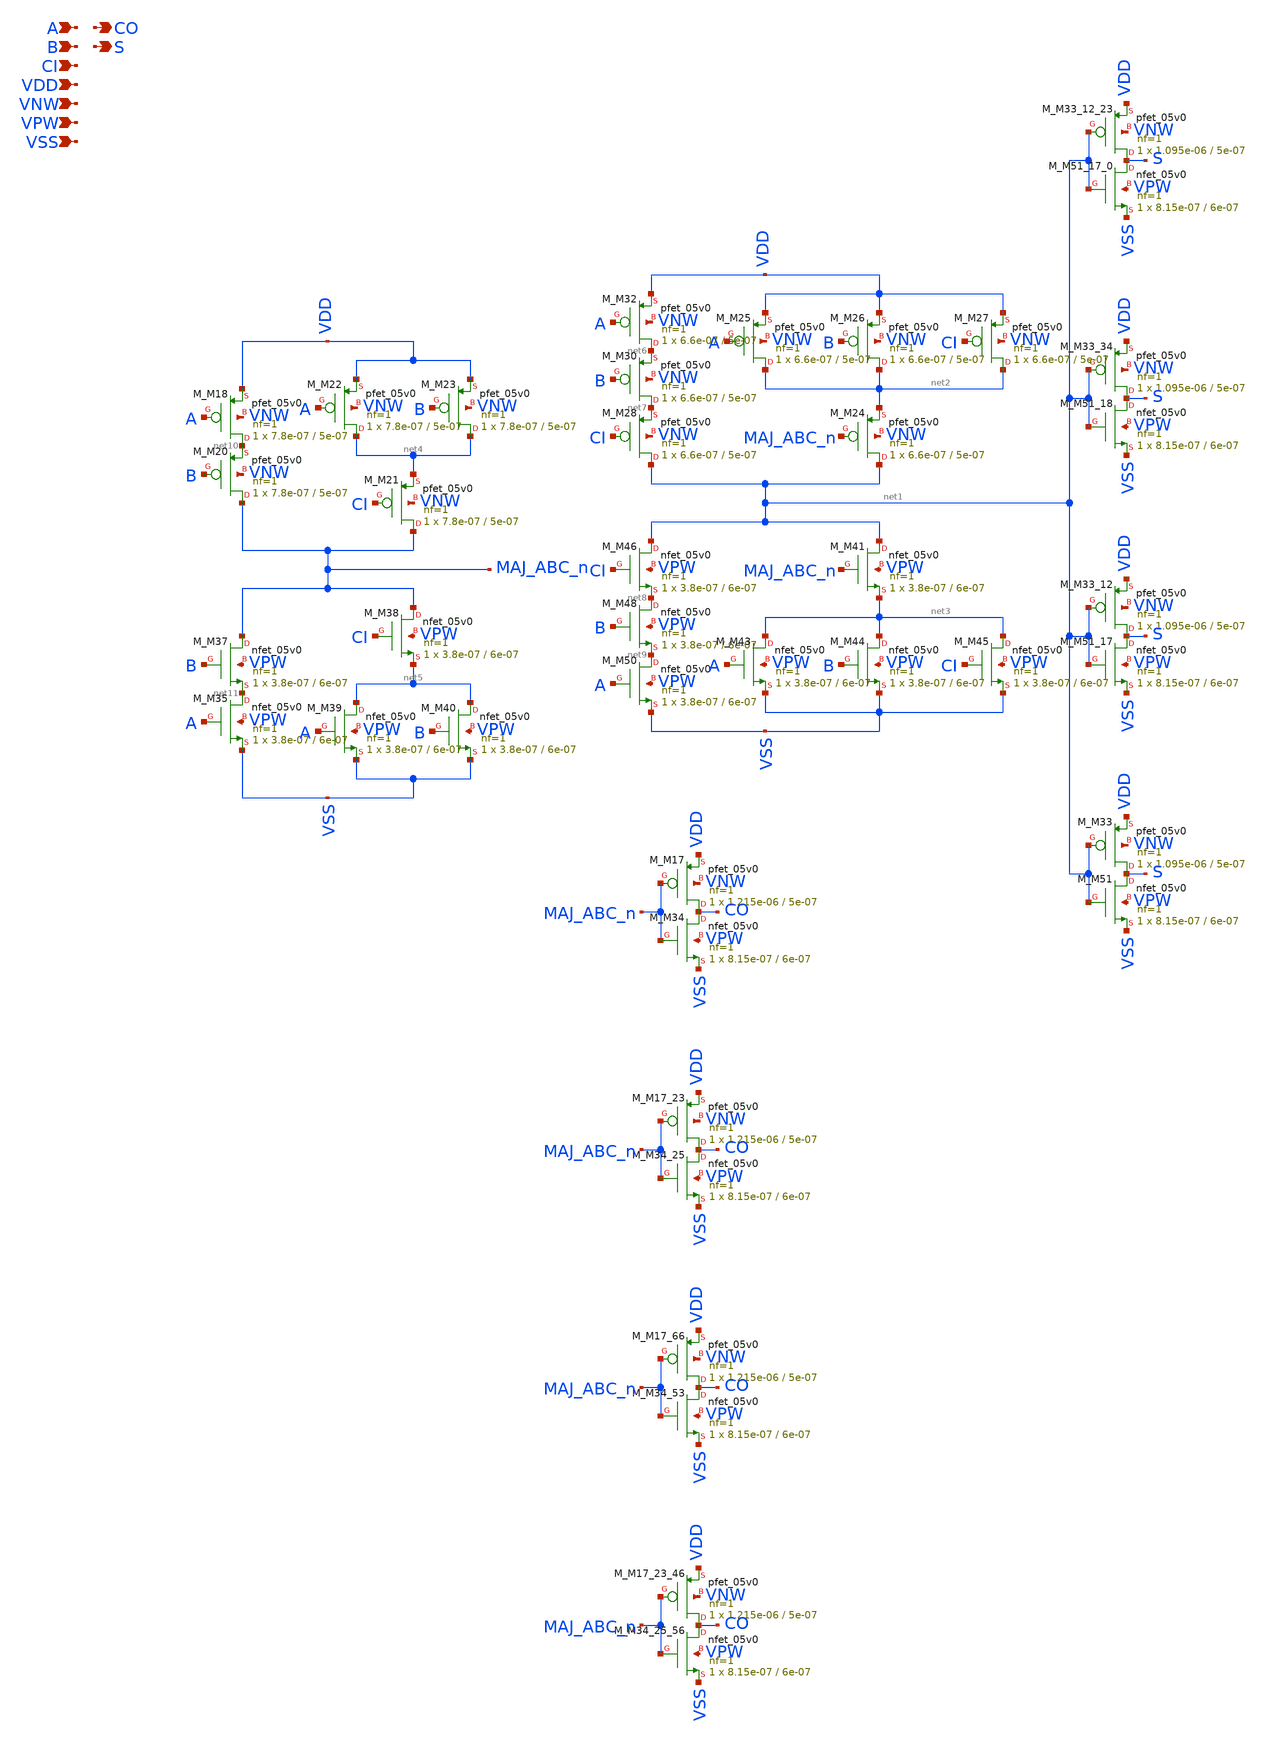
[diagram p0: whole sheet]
** sch_path: schematics/addf/gf180mcu_fd_sc_mcu7t5v0__addf_4.sch
**.subckt gf180mcu_fd_sc_mcu7t5v0__addf_4 A B CI CO S VDD VNW VPW VSS
*.ipin A
*.ipin B
*.ipin CI
*.opin CO
*.opin S
*.ipin VDD
*.ipin VNW
*.ipin VPW
*.ipin VSS
M_M33_12_23 S net1 VDD VNW pfet_05v0 L=5e-07 W=1.095e-06 nf=1 ad='int((nf+1)/2) * W/nf * 0.18u' as='int((nf+2)/2) * W/nf * 0.18u'
+ pd='2*int((nf+1)/2) * (W/nf + 0.18u)' ps='2*int((nf+2)/2) * (W/nf + 0.18u)' nrd='0.18u / W' nrs='0.18u / W'
+ sa=0 sb=0 sd=0 m=1
M_M51_17_0 S net1 VSS VPW nfet_05v0 L=6e-07 W=8.15e-07 nf=1 ad='int((nf+1)/2) * W/nf * 0.18u' as='int((nf+2)/2) * W/nf * 0.18u'
+ pd='2*int((nf+1)/2) * (W/nf + 0.18u)' ps='2*int((nf+2)/2) * (W/nf + 0.18u)' nrd='0.18u / W' nrs='0.18u / W'
+ sa=0 sb=0 sd=0 m=1
M_M33_34 S net1 VDD VNW pfet_05v0 L=5e-07 W=1.095e-06 nf=1 ad='int((nf+1)/2) * W/nf * 0.18u' as='int((nf+2)/2) * W/nf * 0.18u'
+ pd='2*int((nf+1)/2) * (W/nf + 0.18u)' ps='2*int((nf+2)/2) * (W/nf + 0.18u)' nrd='0.18u / W' nrs='0.18u / W'
+ sa=0 sb=0 sd=0 m=1
M_M51_18 S net1 VSS VPW nfet_05v0 L=6e-07 W=8.15e-07 nf=1 ad='int((nf+1)/2) * W/nf * 0.18u' as='int((nf+2)/2) * W/nf * 0.18u'
+ pd='2*int((nf+1)/2) * (W/nf + 0.18u)' ps='2*int((nf+2)/2) * (W/nf + 0.18u)' nrd='0.18u / W' nrs='0.18u / W'
+ sa=0 sb=0 sd=0 m=1
M_M33_12 S net1 VDD VNW pfet_05v0 L=5e-07 W=1.095e-06 nf=1 ad='int((nf+1)/2) * W/nf * 0.18u' as='int((nf+2)/2) * W/nf * 0.18u'
+ pd='2*int((nf+1)/2) * (W/nf + 0.18u)' ps='2*int((nf+2)/2) * (W/nf + 0.18u)' nrd='0.18u / W' nrs='0.18u / W'
+ sa=0 sb=0 sd=0 m=1
M_M51_17 S net1 VSS VPW nfet_05v0 L=6e-07 W=8.15e-07 nf=1 ad='int((nf+1)/2) * W/nf * 0.18u' as='int((nf+2)/2) * W/nf * 0.18u'
+ pd='2*int((nf+1)/2) * (W/nf + 0.18u)' ps='2*int((nf+2)/2) * (W/nf + 0.18u)' nrd='0.18u / W' nrs='0.18u / W'
+ sa=0 sb=0 sd=0 m=1
M_M33 S net1 VDD VNW pfet_05v0 L=5e-07 W=1.095e-06 nf=1 ad='int((nf+1)/2) * W/nf * 0.18u' as='int((nf+2)/2) * W/nf * 0.18u'
+ pd='2*int((nf+1)/2) * (W/nf + 0.18u)' ps='2*int((nf+2)/2) * (W/nf + 0.18u)' nrd='0.18u / W' nrs='0.18u / W'
+ sa=0 sb=0 sd=0 m=1
M_M51 S net1 VSS VPW nfet_05v0 L=6e-07 W=8.15e-07 nf=1 ad='int((nf+1)/2) * W/nf * 0.18u' as='int((nf+2)/2) * W/nf * 0.18u'
+ pd='2*int((nf+1)/2) * (W/nf + 0.18u)' ps='2*int((nf+2)/2) * (W/nf + 0.18u)' nrd='0.18u / W' nrs='0.18u / W'
+ sa=0 sb=0 sd=0 m=1
M_M32 net6 A VDD VNW pfet_05v0 L=5e-07 W=6.6e-07 nf=1 ad='int((nf+1)/2) * W/nf * 0.18u' as='int((nf+2)/2) * W/nf * 0.18u'
+ pd='2*int((nf+1)/2) * (W/nf + 0.18u)' ps='2*int((nf+2)/2) * (W/nf + 0.18u)' nrd='0.18u / W' nrs='0.18u / W'
+ sa=0 sb=0 sd=0 m=1
M_M30 net7 B net6 VNW pfet_05v0 L=5e-07 W=6.6e-07 nf=1 ad='int((nf+1)/2) * W/nf * 0.18u' as='int((nf+2)/2) * W/nf * 0.18u'
+ pd='2*int((nf+1)/2) * (W/nf + 0.18u)' ps='2*int((nf+2)/2) * (W/nf + 0.18u)' nrd='0.18u / W' nrs='0.18u / W'
+ sa=0 sb=0 sd=0 m=1
M_M28 net1 CI net7 VNW pfet_05v0 L=5e-07 W=6.6e-07 nf=1 ad='int((nf+1)/2) * W/nf * 0.18u' as='int((nf+2)/2) * W/nf * 0.18u'
+ pd='2*int((nf+1)/2) * (W/nf + 0.18u)' ps='2*int((nf+2)/2) * (W/nf + 0.18u)' nrd='0.18u / W' nrs='0.18u / W'
+ sa=0 sb=0 sd=0 m=1
M_M25 net2 A VDD VNW pfet_05v0 L=5e-07 W=6.6e-07 nf=1 ad='int((nf+1)/2) * W/nf * 0.18u' as='int((nf+2)/2) * W/nf * 0.18u'
+ pd='2*int((nf+1)/2) * (W/nf + 0.18u)' ps='2*int((nf+2)/2) * (W/nf + 0.18u)' nrd='0.18u / W' nrs='0.18u / W'
+ sa=0 sb=0 sd=0 m=1
M_M26 net2 B VDD VNW pfet_05v0 L=5e-07 W=6.6e-07 nf=1 ad='int((nf+1)/2) * W/nf * 0.18u' as='int((nf+2)/2) * W/nf * 0.18u'
+ pd='2*int((nf+1)/2) * (W/nf + 0.18u)' ps='2*int((nf+2)/2) * (W/nf + 0.18u)' nrd='0.18u / W' nrs='0.18u / W'
+ sa=0 sb=0 sd=0 m=1
M_M27 net2 CI VDD VNW pfet_05v0 L=5e-07 W=6.6e-07 nf=1 ad='int((nf+1)/2) * W/nf * 0.18u' as='int((nf+2)/2) * W/nf * 0.18u'
+ pd='2*int((nf+1)/2) * (W/nf + 0.18u)' ps='2*int((nf+2)/2) * (W/nf + 0.18u)' nrd='0.18u / W' nrs='0.18u / W'
+ sa=0 sb=0 sd=0 m=1
M_M24 net1 MAJ_ABC_n net2 VNW pfet_05v0 L=5e-07 W=6.6e-07 nf=1 ad='int((nf+1)/2) * W/nf * 0.18u' as='int((nf+2)/2) * W/nf * 0.18u'
+ pd='2*int((nf+1)/2) * (W/nf + 0.18u)' ps='2*int((nf+2)/2) * (W/nf + 0.18u)' nrd='0.18u / W' nrs='0.18u / W'
+ sa=0 sb=0 sd=0 m=1
M_M46 net1 CI net8 VPW nfet_05v0 L=6e-07 W=3.8e-07 nf=1 ad='int((nf+1)/2) * W/nf * 0.18u' as='int((nf+2)/2) * W/nf * 0.18u'
+ pd='2*int((nf+1)/2) * (W/nf + 0.18u)' ps='2*int((nf+2)/2) * (W/nf + 0.18u)' nrd='0.18u / W' nrs='0.18u / W'
+ sa=0 sb=0 sd=0 m=1
M_M48 net8 B net9 VPW nfet_05v0 L=6e-07 W=3.8e-07 nf=1 ad='int((nf+1)/2) * W/nf * 0.18u' as='int((nf+2)/2) * W/nf * 0.18u'
+ pd='2*int((nf+1)/2) * (W/nf + 0.18u)' ps='2*int((nf+2)/2) * (W/nf + 0.18u)' nrd='0.18u / W' nrs='0.18u / W'
+ sa=0 sb=0 sd=0 m=1
M_M50 net9 A VSS VPW nfet_05v0 L=6e-07 W=3.8e-07 nf=1 ad='int((nf+1)/2) * W/nf * 0.18u' as='int((nf+2)/2) * W/nf * 0.18u'
+ pd='2*int((nf+1)/2) * (W/nf + 0.18u)' ps='2*int((nf+2)/2) * (W/nf + 0.18u)' nrd='0.18u / W' nrs='0.18u / W'
+ sa=0 sb=0 sd=0 m=1
M_M41 net1 MAJ_ABC_n net3 VPW nfet_05v0 L=6e-07 W=3.8e-07 nf=1 ad='int((nf+1)/2) * W/nf * 0.18u' as='int((nf+2)/2) * W/nf * 0.18u'
+ pd='2*int((nf+1)/2) * (W/nf + 0.18u)' ps='2*int((nf+2)/2) * (W/nf + 0.18u)' nrd='0.18u / W' nrs='0.18u / W'
+ sa=0 sb=0 sd=0 m=1
M_M43 net3 A VSS VPW nfet_05v0 L=6e-07 W=3.8e-07 nf=1 ad='int((nf+1)/2) * W/nf * 0.18u' as='int((nf+2)/2) * W/nf * 0.18u'
+ pd='2*int((nf+1)/2) * (W/nf + 0.18u)' ps='2*int((nf+2)/2) * (W/nf + 0.18u)' nrd='0.18u / W' nrs='0.18u / W'
+ sa=0 sb=0 sd=0 m=1
M_M44 net3 B VSS VPW nfet_05v0 L=6e-07 W=3.8e-07 nf=1 ad='int((nf+1)/2) * W/nf * 0.18u' as='int((nf+2)/2) * W/nf * 0.18u'
+ pd='2*int((nf+1)/2) * (W/nf + 0.18u)' ps='2*int((nf+2)/2) * (W/nf + 0.18u)' nrd='0.18u / W' nrs='0.18u / W'
+ sa=0 sb=0 sd=0 m=1
M_M45 net3 CI VSS VPW nfet_05v0 L=6e-07 W=3.8e-07 nf=1 ad='int((nf+1)/2) * W/nf * 0.18u' as='int((nf+2)/2) * W/nf * 0.18u'
+ pd='2*int((nf+1)/2) * (W/nf + 0.18u)' ps='2*int((nf+2)/2) * (W/nf + 0.18u)' nrd='0.18u / W' nrs='0.18u / W'
+ sa=0 sb=0 sd=0 m=1
M_M18 net10 A VDD VNW pfet_05v0 L=5e-07 W=7.8e-07 nf=1 ad='int((nf+1)/2) * W/nf * 0.18u' as='int((nf+2)/2) * W/nf * 0.18u'
+ pd='2*int((nf+1)/2) * (W/nf + 0.18u)' ps='2*int((nf+2)/2) * (W/nf + 0.18u)' nrd='0.18u / W' nrs='0.18u / W'
+ sa=0 sb=0 sd=0 m=1
M_M20 MAJ_ABC_n B net10 VNW pfet_05v0 L=5e-07 W=7.8e-07 nf=1 ad='int((nf+1)/2) * W/nf * 0.18u' as='int((nf+2)/2) * W/nf * 0.18u'
+ pd='2*int((nf+1)/2) * (W/nf + 0.18u)' ps='2*int((nf+2)/2) * (W/nf + 0.18u)' nrd='0.18u / W' nrs='0.18u / W'
+ sa=0 sb=0 sd=0 m=1
M_M22 net4 A VDD VNW pfet_05v0 L=5e-07 W=7.8e-07 nf=1 ad='int((nf+1)/2) * W/nf * 0.18u' as='int((nf+2)/2) * W/nf * 0.18u'
+ pd='2*int((nf+1)/2) * (W/nf + 0.18u)' ps='2*int((nf+2)/2) * (W/nf + 0.18u)' nrd='0.18u / W' nrs='0.18u / W'
+ sa=0 sb=0 sd=0 m=1
M_M23 net4 B VDD VNW pfet_05v0 L=5e-07 W=7.8e-07 nf=1 ad='int((nf+1)/2) * W/nf * 0.18u' as='int((nf+2)/2) * W/nf * 0.18u'
+ pd='2*int((nf+1)/2) * (W/nf + 0.18u)' ps='2*int((nf+2)/2) * (W/nf + 0.18u)' nrd='0.18u / W' nrs='0.18u / W'
+ sa=0 sb=0 sd=0 m=1
M_M21 MAJ_ABC_n CI net4 VNW pfet_05v0 L=5e-07 W=7.8e-07 nf=1 ad='int((nf+1)/2) * W/nf * 0.18u' as='int((nf+2)/2) * W/nf * 0.18u'
+ pd='2*int((nf+1)/2) * (W/nf + 0.18u)' ps='2*int((nf+2)/2) * (W/nf + 0.18u)' nrd='0.18u / W' nrs='0.18u / W'
+ sa=0 sb=0 sd=0 m=1
M_M37 MAJ_ABC_n B net11 VPW nfet_05v0 L=6e-07 W=3.8e-07 nf=1 ad='int((nf+1)/2) * W/nf * 0.18u' as='int((nf+2)/2) * W/nf * 0.18u'
+ pd='2*int((nf+1)/2) * (W/nf + 0.18u)' ps='2*int((nf+2)/2) * (W/nf + 0.18u)' nrd='0.18u / W' nrs='0.18u / W'
+ sa=0 sb=0 sd=0 m=1
M_M35 net11 A VSS VPW nfet_05v0 L=6e-07 W=3.8e-07 nf=1 ad='int((nf+1)/2) * W/nf * 0.18u' as='int((nf+2)/2) * W/nf * 0.18u'
+ pd='2*int((nf+1)/2) * (W/nf + 0.18u)' ps='2*int((nf+2)/2) * (W/nf + 0.18u)' nrd='0.18u / W' nrs='0.18u / W'
+ sa=0 sb=0 sd=0 m=1
M_M38 MAJ_ABC_n CI net5 VPW nfet_05v0 L=6e-07 W=3.8e-07 nf=1 ad='int((nf+1)/2) * W/nf * 0.18u' as='int((nf+2)/2) * W/nf * 0.18u'
+ pd='2*int((nf+1)/2) * (W/nf + 0.18u)' ps='2*int((nf+2)/2) * (W/nf + 0.18u)' nrd='0.18u / W' nrs='0.18u / W'
+ sa=0 sb=0 sd=0 m=1
M_M39 net5 A VSS VPW nfet_05v0 L=6e-07 W=3.8e-07 nf=1 ad='int((nf+1)/2) * W/nf * 0.18u' as='int((nf+2)/2) * W/nf * 0.18u'
+ pd='2*int((nf+1)/2) * (W/nf + 0.18u)' ps='2*int((nf+2)/2) * (W/nf + 0.18u)' nrd='0.18u / W' nrs='0.18u / W'
+ sa=0 sb=0 sd=0 m=1
M_M40 net5 B VSS VPW nfet_05v0 L=6e-07 W=3.8e-07 nf=1 ad='int((nf+1)/2) * W/nf * 0.18u' as='int((nf+2)/2) * W/nf * 0.18u'
+ pd='2*int((nf+1)/2) * (W/nf + 0.18u)' ps='2*int((nf+2)/2) * (W/nf + 0.18u)' nrd='0.18u / W' nrs='0.18u / W'
+ sa=0 sb=0 sd=0 m=1
M_M17 CO MAJ_ABC_n VDD VNW pfet_05v0 L=5e-07 W=1.215e-06 nf=1 ad='int((nf+1)/2) * W/nf * 0.18u' as='int((nf+2)/2) * W/nf * 0.18u'
+ pd='2*int((nf+1)/2) * (W/nf + 0.18u)' ps='2*int((nf+2)/2) * (W/nf + 0.18u)' nrd='0.18u / W' nrs='0.18u / W'
+ sa=0 sb=0 sd=0 m=1
M_M34 CO MAJ_ABC_n VSS VPW nfet_05v0 L=6e-07 W=8.15e-07 nf=1 ad='int((nf+1)/2) * W/nf * 0.18u' as='int((nf+2)/2) * W/nf * 0.18u'
+ pd='2*int((nf+1)/2) * (W/nf + 0.18u)' ps='2*int((nf+2)/2) * (W/nf + 0.18u)' nrd='0.18u / W' nrs='0.18u / W'
+ sa=0 sb=0 sd=0 m=1
M_M17_23 CO MAJ_ABC_n VDD VNW pfet_05v0 L=5e-07 W=1.215e-06 nf=1 ad='int((nf+1)/2) * W/nf * 0.18u' as='int((nf+2)/2) * W/nf * 0.18u'
+ pd='2*int((nf+1)/2) * (W/nf + 0.18u)' ps='2*int((nf+2)/2) * (W/nf + 0.18u)' nrd='0.18u / W' nrs='0.18u / W'
+ sa=0 sb=0 sd=0 m=1
M_M34_25 CO MAJ_ABC_n VSS VPW nfet_05v0 L=6e-07 W=8.15e-07 nf=1 ad='int((nf+1)/2) * W/nf * 0.18u' as='int((nf+2)/2) * W/nf * 0.18u'
+ pd='2*int((nf+1)/2) * (W/nf + 0.18u)' ps='2*int((nf+2)/2) * (W/nf + 0.18u)' nrd='0.18u / W' nrs='0.18u / W'
+ sa=0 sb=0 sd=0 m=1
M_M17_66 CO MAJ_ABC_n VDD VNW pfet_05v0 L=5e-07 W=1.215e-06 nf=1 ad='int((nf+1)/2) * W/nf * 0.18u' as='int((nf+2)/2) * W/nf * 0.18u'
+ pd='2*int((nf+1)/2) * (W/nf + 0.18u)' ps='2*int((nf+2)/2) * (W/nf + 0.18u)' nrd='0.18u / W' nrs='0.18u / W'
+ sa=0 sb=0 sd=0 m=1
M_M34_53 CO MAJ_ABC_n VSS VPW nfet_05v0 L=6e-07 W=8.15e-07 nf=1 ad='int((nf+1)/2) * W/nf * 0.18u' as='int((nf+2)/2) * W/nf * 0.18u'
+ pd='2*int((nf+1)/2) * (W/nf + 0.18u)' ps='2*int((nf+2)/2) * (W/nf + 0.18u)' nrd='0.18u / W' nrs='0.18u / W'
+ sa=0 sb=0 sd=0 m=1
M_M17_23_46 CO MAJ_ABC_n VDD VNW pfet_05v0 L=5e-07 W=1.215e-06 nf=1 ad='int((nf+1)/2) * W/nf * 0.18u'
+ as='int((nf+2)/2) * W/nf * 0.18u' pd='2*int((nf+1)/2) * (W/nf + 0.18u)' ps='2*int((nf+2)/2) * (W/nf + 0.18u)'
+ nrd='0.18u / W' nrs='0.18u / W' sa=0 sb=0 sd=0 m=1
M_M34_25_56 CO MAJ_ABC_n VSS VPW nfet_05v0 L=6e-07 W=8.15e-07 nf=1 ad='int((nf+1)/2) * W/nf * 0.18u'
+ as='int((nf+2)/2) * W/nf * 0.18u' pd='2*int((nf+1)/2) * (W/nf + 0.18u)' ps='2*int((nf+2)/2) * (W/nf + 0.18u)'
+ nrd='0.18u / W' nrs='0.18u / W' sa=0 sb=0 sd=0 m=1
**.ends
.end
